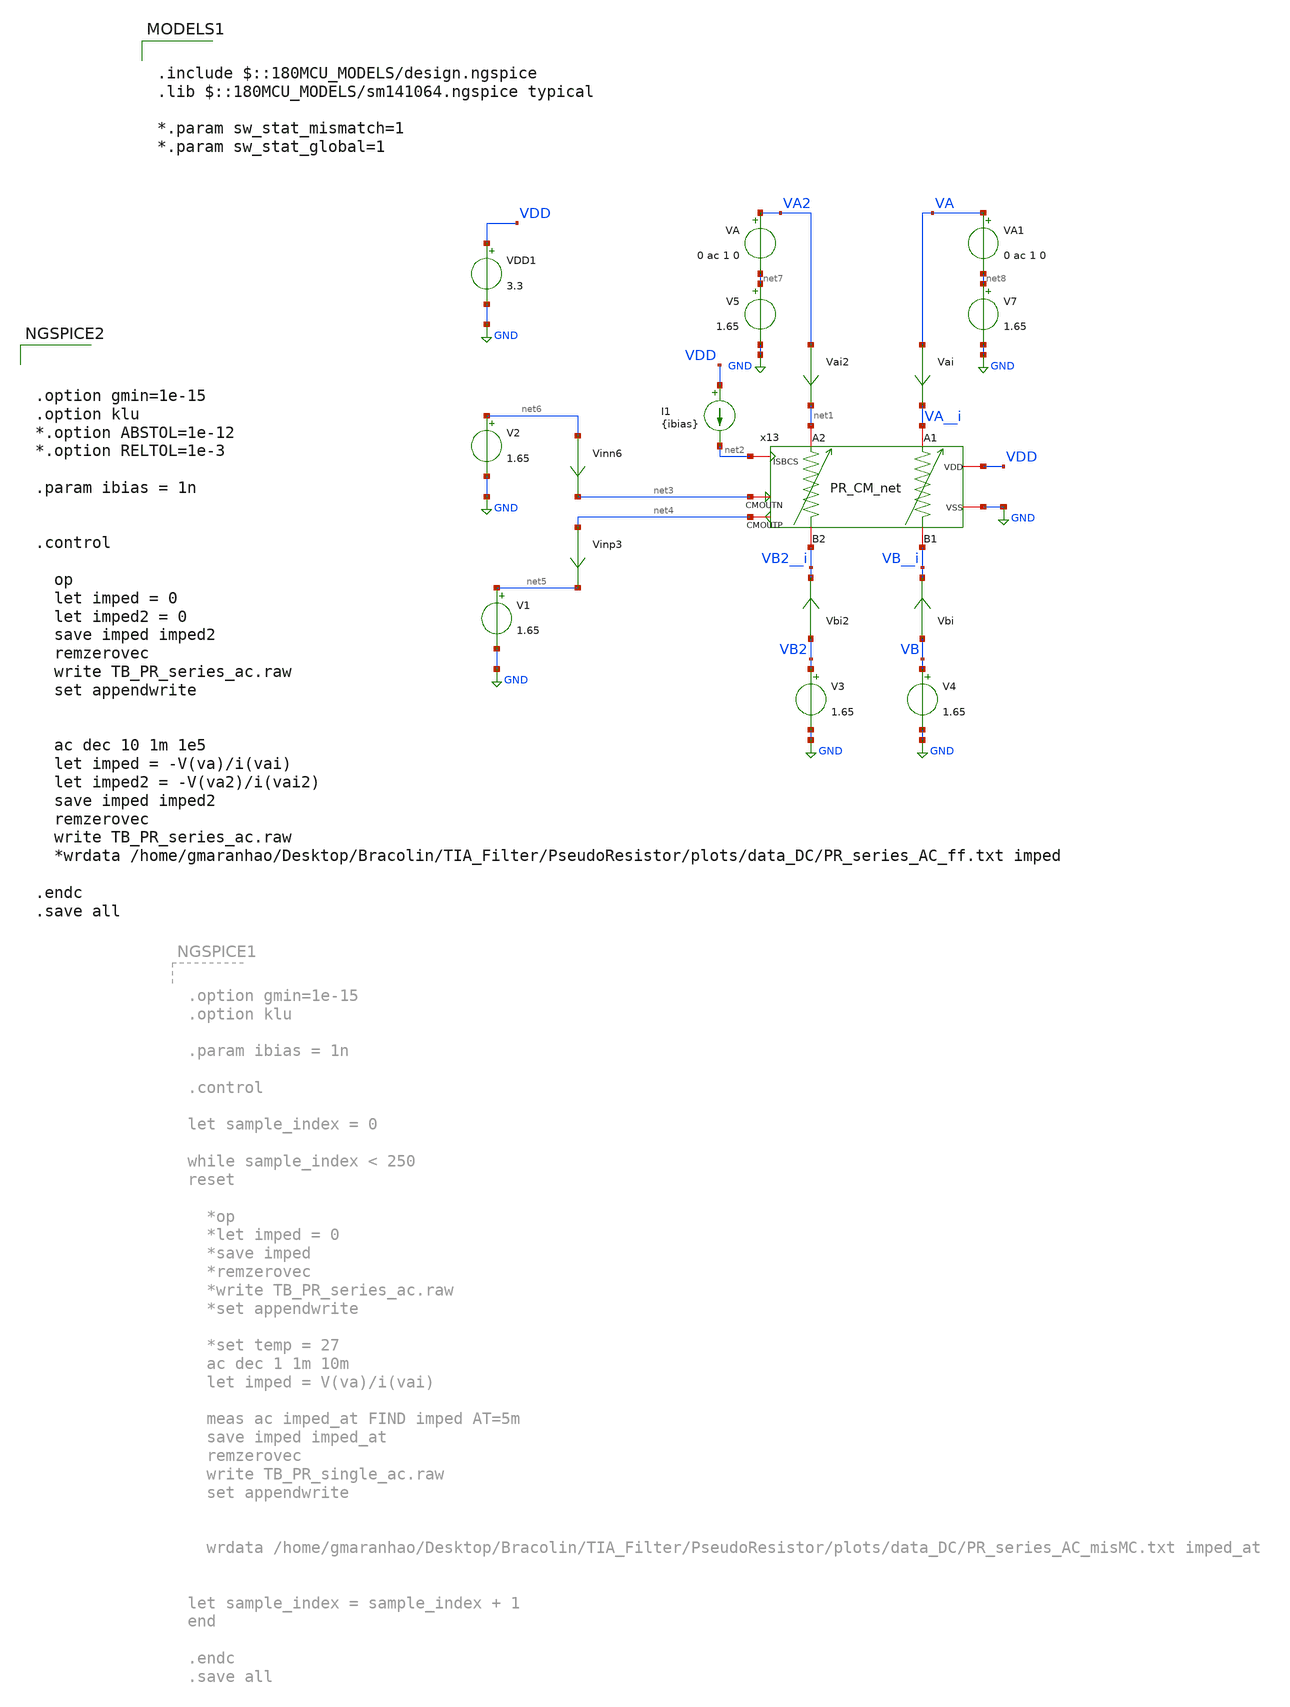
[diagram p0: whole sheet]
** sch_path: TIA_Filter/PseudoResistor/TB_PR_series_ac.sch
**.subckt TB_PR_series_ac
Vai VA VA__i 0
.save i(vai)
Vbi VB VB__i 0
.save i(vbi)
Vbi2 VB2 VB2__i 0
.save i(vbi2)
Vai2 VA2 net1 0
.save i(vai2)
x13 net2 VA__i net1 VB2__i VB__i net3 net4 VDD GND PR_CM_net
I1 VDD net2 {ibias}
Vinn6 net6 net3 0
.save i(vinn6)
Vinp3 net4 net5 0
.save i(vinp3)
V1 net5 GND 1.65
V2 net6 GND 1.65
V3 VB2 GND 1.65
V4 VB GND 1.65
V5 net7 GND 1.65
V7 net8 GND 1.65
VA VA2 net7 0 ac 1 0
VA1 VA net8 0 ac 1 0
VDD1 VDD GND 3.3
**** begin user architecture code



.option gmin=1e-15
.option klu
*.option ABSTOL=1e-12
*.option RELTOL=1e-3

.param ibias = 1n


.control

  op
  let imped = 0
  let imped2 = 0
  save imped imped2
  remzerovec
  write TB_PR_series_ac.raw
  set appendwrite


  ac dec 10 1m 1e5
  let imped = -V(va)/i(vai)
  let imped2 = -V(va2)/i(vai2)
  save imped imped2
  remzerovec
  write TB_PR_series_ac.raw
  *wrdata
+ /home/gmaranhao/Desktop/Bracolin/TIA_Filter/PseudoResistor/plots/data_DC/PR_series_AC_ff.txt imped

.endc
.save all



.include $::180MCU_MODELS/design.ngspice
.lib $::180MCU_MODELS/sm141064.ngspice typical

*.param sw_stat_mismatch=1
*.param sw_stat_global=1


**** end user architecture code
**.ends
.GLOBAL GND
.end
